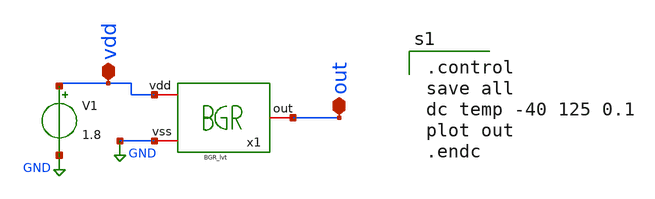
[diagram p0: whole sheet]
** sch_path: OTHER_SOLUTIONS_CONSIDERED/OTHER_BIAS_FOR_TEMPERATURE_SENSOR/BGR/XSCHEM/BGR_lvt_tb.sch
**.subckt BGR_lvt_tb out vdd
*.iopin out
*.iopin vdd
V1 net1 GND 1.8
x1 vdd out GND BGR_lvt
**** begin user architecture code

.control
save all
dc temp -40 125 0.1
plot out
.endc


** opencircuitdesign pdks install
.lib $::SKYWATER_MODELS/sky130.lib.spice tt


**** end user architecture code
**.ends
.GLOBAL GND
.end
